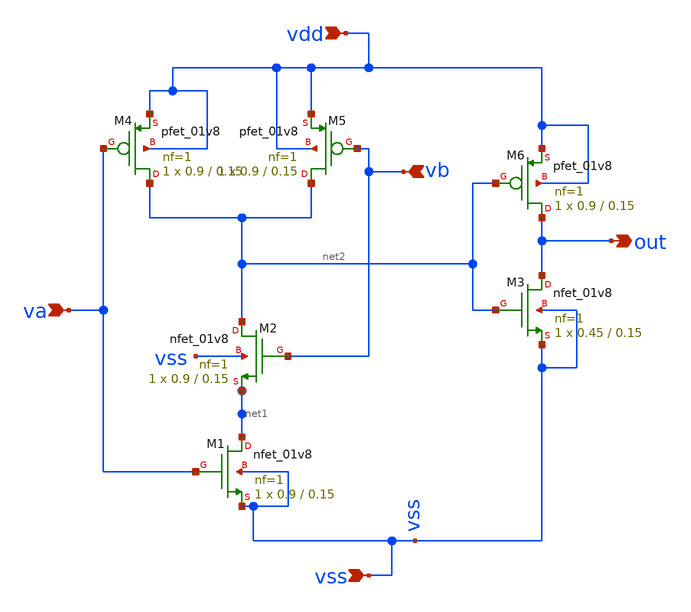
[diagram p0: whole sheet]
** sch_path: track_vlsi/toplevel_vlsi/sch/and_lafe.sch
**.subckt and_lafe out va vb vdd vss
*.opin out
*.ipin va
*.ipin vb
*.ipin vdd
*.ipin vss
XM1 net1 va vss vss sky130_fd_pr__nfet_01v8 L=0.15 W=0.9 nf=1 ad='int((nf+1)/2) * W/nf * 0.29' as='int((nf+2)/2) * W/nf * 0.29'
+ pd='2*int((nf+1)/2) * (W/nf + 0.29)' ps='2*int((nf+2)/2) * (W/nf + 0.29)' nrd='0.29 / W' nrs='0.29 / W'
+ sa=0 sb=0 sd=0 mult=1 m=1
XM2 net2 vb net1 vss sky130_fd_pr__nfet_01v8 L=0.15 W=0.9 nf=1 ad='int((nf+1)/2) * W/nf * 0.29' as='int((nf+2)/2) * W/nf * 0.29'
+ pd='2*int((nf+1)/2) * (W/nf + 0.29)' ps='2*int((nf+2)/2) * (W/nf + 0.29)' nrd='0.29 / W' nrs='0.29 / W'
+ sa=0 sb=0 sd=0 mult=1 m=1
XM3 out net2 vss vss sky130_fd_pr__nfet_01v8 L=0.15 W=0.45 nf=1 ad='int((nf+1)/2) * W/nf * 0.29' as='int((nf+2)/2) * W/nf * 0.29'
+ pd='2*int((nf+1)/2) * (W/nf + 0.29)' ps='2*int((nf+2)/2) * (W/nf + 0.29)' nrd='0.29 / W' nrs='0.29 / W'
+ sa=0 sb=0 sd=0 mult=1 m=1
XM4 net2 va vdd vdd sky130_fd_pr__pfet_01v8 L=0.15 W=0.9 nf=1 ad='int((nf+1)/2) * W/nf * 0.29' as='int((nf+2)/2) * W/nf * 0.29'
+ pd='2*int((nf+1)/2) * (W/nf + 0.29)' ps='2*int((nf+2)/2) * (W/nf + 0.29)' nrd='0.29 / W' nrs='0.29 / W'
+ sa=0 sb=0 sd=0 mult=1 m=1
XM5 net2 vb vdd vdd sky130_fd_pr__pfet_01v8 L=0.15 W=0.9 nf=1 ad='int((nf+1)/2) * W/nf * 0.29' as='int((nf+2)/2) * W/nf * 0.29'
+ pd='2*int((nf+1)/2) * (W/nf + 0.29)' ps='2*int((nf+2)/2) * (W/nf + 0.29)' nrd='0.29 / W' nrs='0.29 / W'
+ sa=0 sb=0 sd=0 mult=1 m=1
XM6 out net2 vdd vdd sky130_fd_pr__pfet_01v8 L=0.15 W=0.9 nf=1 ad='int((nf+1)/2) * W/nf * 0.29' as='int((nf+2)/2) * W/nf * 0.29'
+ pd='2*int((nf+1)/2) * (W/nf + 0.29)' ps='2*int((nf+2)/2) * (W/nf + 0.29)' nrd='0.29 / W' nrs='0.29 / W'
+ sa=0 sb=0 sd=0 mult=1 m=1
**.ends
.end
